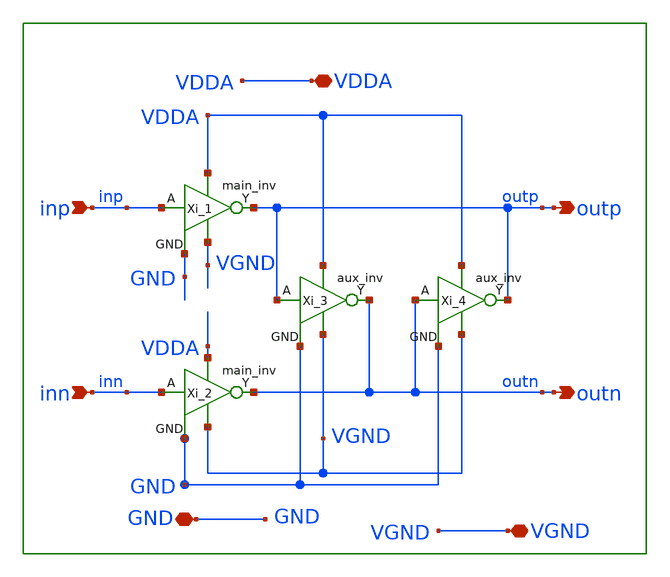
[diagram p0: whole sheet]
** sch_path: xschem/lib/cc_inv.sch
**.subckt cc_inv outp inn VGND outn inp VDDA GND
*.opin outp
*.ipin inn
*.iopin VGND
*.opin outn
*.ipin inp
*.iopin VDDA
*.iopin GND
Xi_1 inp outp VGND VDDA GND main_inv
Xi_2 inn outn VGND VDDA GND main_inv
Xi_3 VDDA VGND outn GND outp aux_inv
Xi_4 VDDA VGND outp GND outn aux_inv
**.ends
.end
